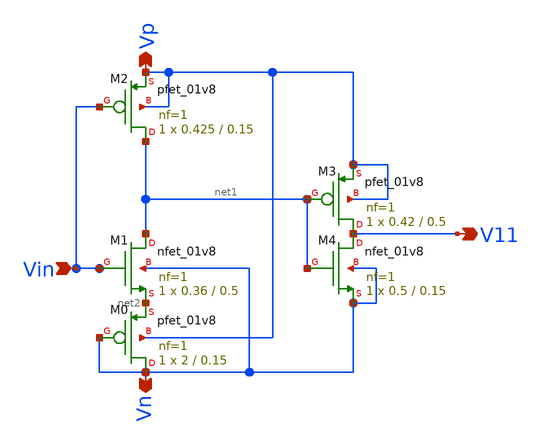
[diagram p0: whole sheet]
** sch_path: xschem/Vth_sch/Symbol/th11.sch
**.subckt th11 Vn Vp Vin V11
*.opin Vn
*.opin Vp
*.ipin Vin
*.opin V11
XM3 V11 net1 Vp Vp sky130_fd_pr__pfet_01v8 L=0.5 W=0.42 nf=1 ad='int((nf+1)/2) * W/nf * 0.29' as='int((nf+2)/2) * W/nf * 0.29'
+ pd='2*int((nf+1)/2) * (W/nf + 0.29)' ps='2*int((nf+2)/2) * (W/nf + 0.29)' nrd='0.29 / W' nrs='0.29 / W'
+ sa=0 sb=0 sd=0 mult=1 m=1
XM4 V11 net1 Vn Vn sky130_fd_pr__nfet_01v8 L=0.15 W=0.5 nf=1 ad='int((nf+1)/2) * W/nf * 0.29' as='int((nf+2)/2) * W/nf * 0.29'
+ pd='2*int((nf+1)/2) * (W/nf + 0.29)' ps='2*int((nf+2)/2) * (W/nf + 0.29)' nrd='0.29 / W' nrs='0.29 / W'
+ sa=0 sb=0 sd=0 mult=1 m=1
XM2 net1 Vin Vp Vp sky130_fd_pr__pfet_01v8 L=0.15 W=0.425 nf=1 ad='int((nf+1)/2) * W/nf * 0.29' as='int((nf+2)/2) * W/nf * 0.29'
+ pd='2*int((nf+1)/2) * (W/nf + 0.29)' ps='2*int((nf+2)/2) * (W/nf + 0.29)' nrd='0.29 / W' nrs='0.29 / W'
+ sa=0 sb=0 sd=0 mult=1 m=1
XM1 net1 Vin net2 Vn sky130_fd_pr__nfet_01v8 L=0.5 W=0.36 nf=1 ad='int((nf+1)/2) * W/nf * 0.29' as='int((nf+2)/2) * W/nf * 0.29'
+ pd='2*int((nf+1)/2) * (W/nf + 0.29)' ps='2*int((nf+2)/2) * (W/nf + 0.29)' nrd='0.29 / W' nrs='0.29 / W'
+ sa=0 sb=0 sd=0 mult=1 m=1
XM0 Vn Vn net2 Vp sky130_fd_pr__pfet_01v8 L=0.15 W=2 nf=1 ad='int((nf+1)/2) * W/nf * 0.29' as='int((nf+2)/2) * W/nf * 0.29'
+ pd='2*int((nf+1)/2) * (W/nf + 0.29)' ps='2*int((nf+2)/2) * (W/nf + 0.29)' nrd='0.29 / W' nrs='0.29 / W'
+ sa=0 sb=0 sd=0 mult=1 m=1
**.ends
.end
